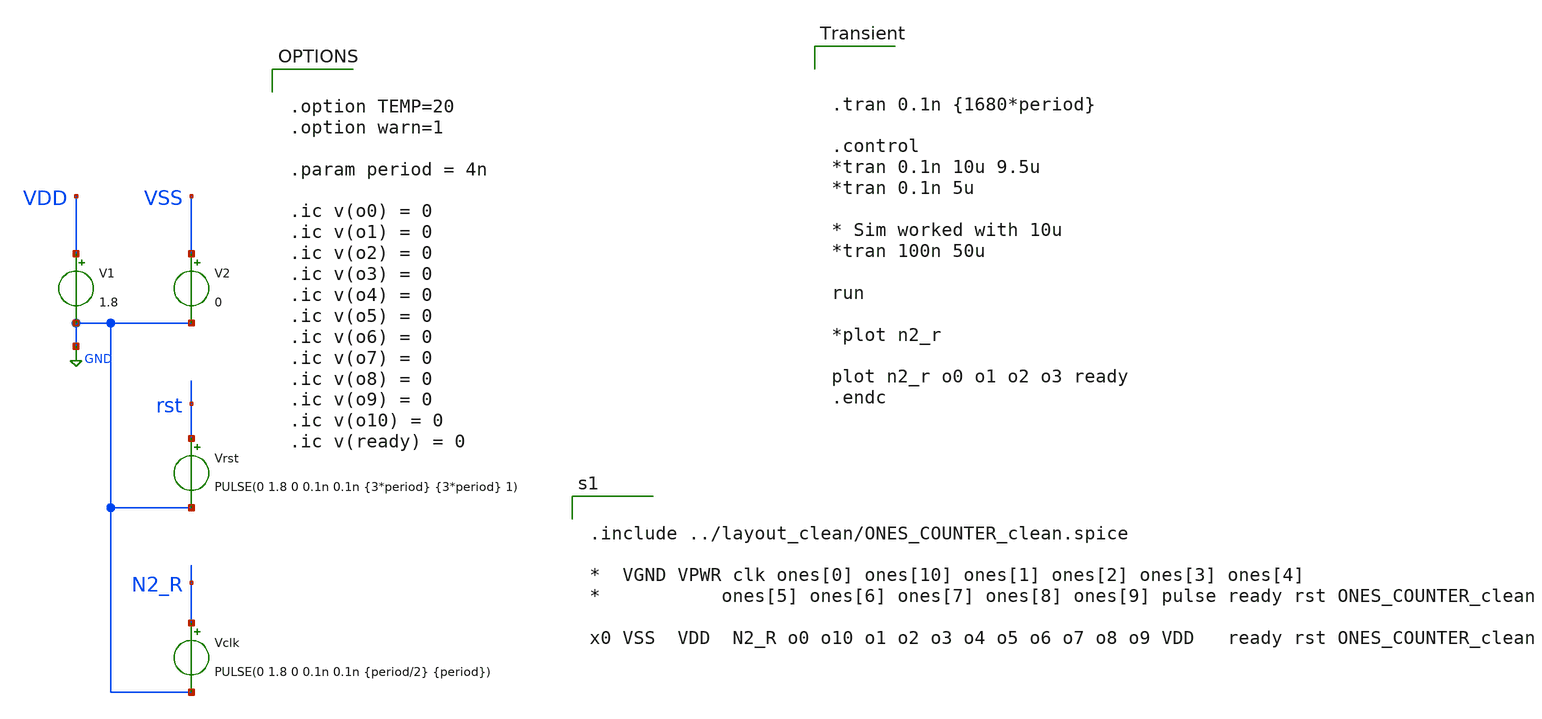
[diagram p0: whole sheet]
** sch_path: modules/ONES_COUNTER/test/only_counter.sch
**.subckt only_counter
V1 VDD GND 1.8
V2 VSS GND 0
Vrst rst GND PULSE(0 1.8 0 0.1n 0.1n {3*period} {3*period} 1)
Vclk N2_R GND PULSE(0 1.8 0 0.1n 0.1n {period/2} {period})
**** begin user architecture code



.tran 0.1n {1680*period}

.control
*tran 0.1n 10u 9.5u
*tran 0.1n 5u

* Sim worked with 10u
*tran 100n 50u

run

*plot n2_r

plot n2_r o0 o1 o2 o3 ready
.endc



.option TEMP=20
.option warn=1

.param period = 4n

.ic v(o0) = 0
.ic v(o1) = 0
.ic v(o2) = 0
.ic v(o3) = 0
.ic v(o4) = 0
.ic v(o5) = 0
.ic v(o6) = 0
.ic v(o7) = 0
.ic v(o8) = 0
.ic v(o9) = 0
.ic v(o10) = 0
.ic v(ready) = 0



.lib $env(PDK_ROOT)/$env(PDK)/libs.tech/combined/sky130.lib.spice tt
*.lib $env(PDK_ROOT)/$env(PDK)/libs.tech/ngspice/sky130.lib.spice tt

*.include $env(PDK_ROOT)/$env(PDK)/libs.ref/sky130_fd_sc_hd/spice/sky130_fd_sc_hd.spice



.include ../layout_clean/ONES_COUNTER_clean.spice

*  VGND VPWR clk ones[0] ones[10] ones[1] ones[2] ones[3] ones[4]
*           ones[5] ones[6] ones[7] ones[8] ones[9] pulse ready rst ONES_COUNTER_clean

x0 VSS  VDD  N2_R o0 o10 o1 o2 o3 o4 o5 o6 o7 o8 o9 VDD   ready rst ONES_COUNTER_clean


**** end user architecture code
**.ends
.GLOBAL GND
.end
